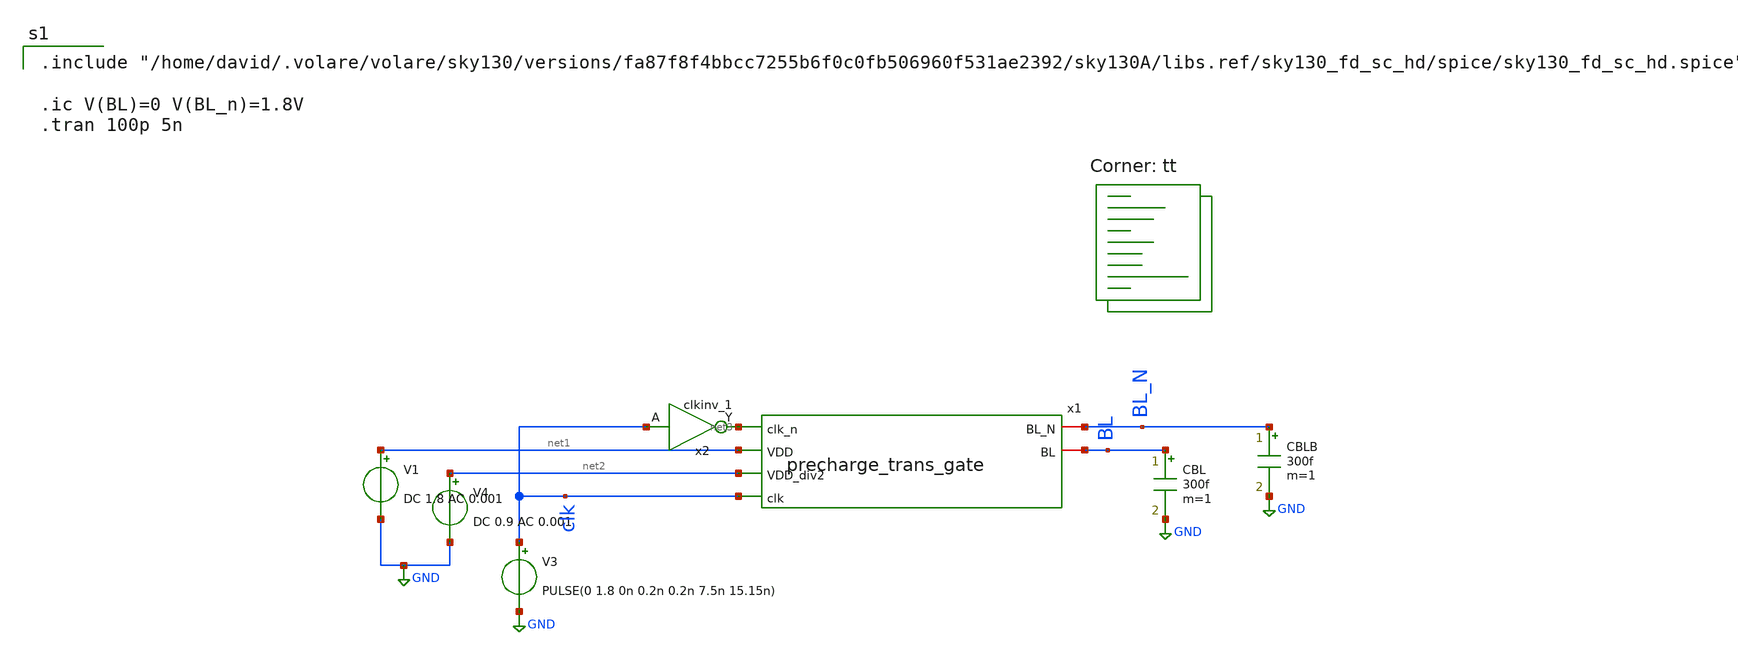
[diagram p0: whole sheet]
** sch_path: analog/schematics/trans_gate_tb.sch
**.subckt trans_gate_tb
V3 clk GND PULSE(0 1.8 0n 0.2n 0.2n 7.5n 15.15n)
x2 clk VGND VNB VPB VPWR net3 sky130_fd_sc_hd__clkinv_1
V4 net2 GND DC 0.9 AC 0.001
CBLB BL_N GND 300f m=1
CBL BL GND 300f m=1
x1 net3 BL_N BL net1 net2 clk precharge_trans_gate
V1 net1 GND DC 1.8 AC 0.001
**** begin user architecture code

.include "/home/david/.volare/volare/sky130/versions/fa87f8f4bbcc7255b6f0c0fb506960f531ae2392/sky130A/libs.ref/sky130_fd_sc_hd/spice/sky130_fd_sc_hd.spice"

.ic V(BL)=0 V(BL_n)=1.8V
.tran 100p 5n

.lib $::SKYWATER_MODELS/sky130.lib.spice tt
**** end user architecture code
**.ends
.GLOBAL GND
.end
